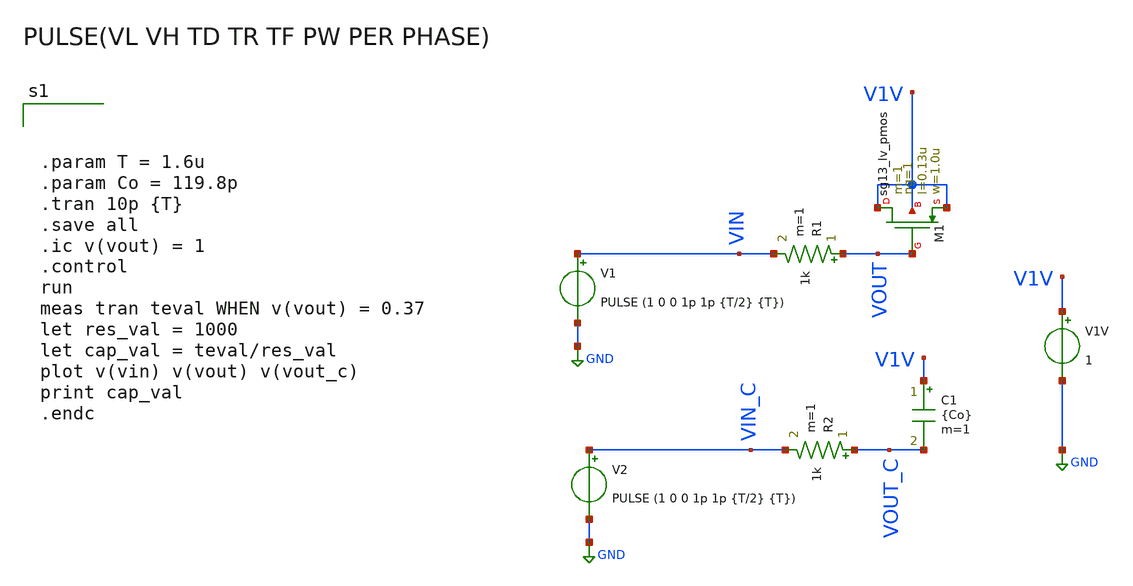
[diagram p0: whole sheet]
** sch_path: xschem/TB/TB_lvPMOS_cgate-ext.sch
**.subckt TB_lvPMOS_cgate-ext
R1 VOUT VIN 1k m=1
V1 VIN GND PULSE (1 0 0 1p 1p {T/2} {T})
V1V V1V GND 1
R2 VOUT_C VIN_C 1k m=1
V2 VIN_C GND PULSE (1 0 0 1p 1p {T/2} {T})
C1 V1V VOUT_C {Co} m=1
XM1 V1V VOUT V1V V1V sg13_lv_pmos w=1.0u l=0.13u ng=1 m=1 mm_ok=1
**** begin user architecture code



.param T = 1.6u
.param Co = 119.8p
.tran 10p {T}
.save all
.ic v(vout) = 1
.control
run
meas tran teval WHEN v(vout) = 0.37
let res_val = 1000
let cap_val = teval/res_val
plot v(vin) v(vout) v(vout_c)
print cap_val
.endc




.lib cornerMOShv.lib mos_tt
.lib cornerMOSlv.lib mos_tt
*.lib cornerMOShv.lib mos_ff
*.lib cornerMOSlv.lib mos_ff
*.lib cornerMOShv.lib mos_ss
*.lib cornerMOSlv.lib mos_ss
*.lib cornerMOShv.lib mos_sf
*.lib cornerMOSlv.lib mos_sf
*.lib cornerMOShv.lib mos_fs
*.lib cornerMOSlv.lib mos_fs

.include /opt/pdks/ihp-sg13g2/libs.ref/sg13g2_stdcell/spice/sg13g2_stdcell.spice
.lib $::SG13G2_MODELS/cornerRES.lib res_typ
.lib $::SG13G2_MODELS/cornerCAP.lib cap_typ
*.lib $::SG13G2_MODELS/diodes.lib



*M1 hvPMOS
.param temp=27
.param mult_M1 = 12000
.param w_M1 =10u
.param l_M1 = 0.4u
.param ng_M1 = 1

*M2 hvNMOS
.param mult_M2 = 4000
.param w_M2 =10u
.param l_M2 =0.45u
.param ng_M2 =1






**** end user architecture code
**.ends
.GLOBAL GND
.end
